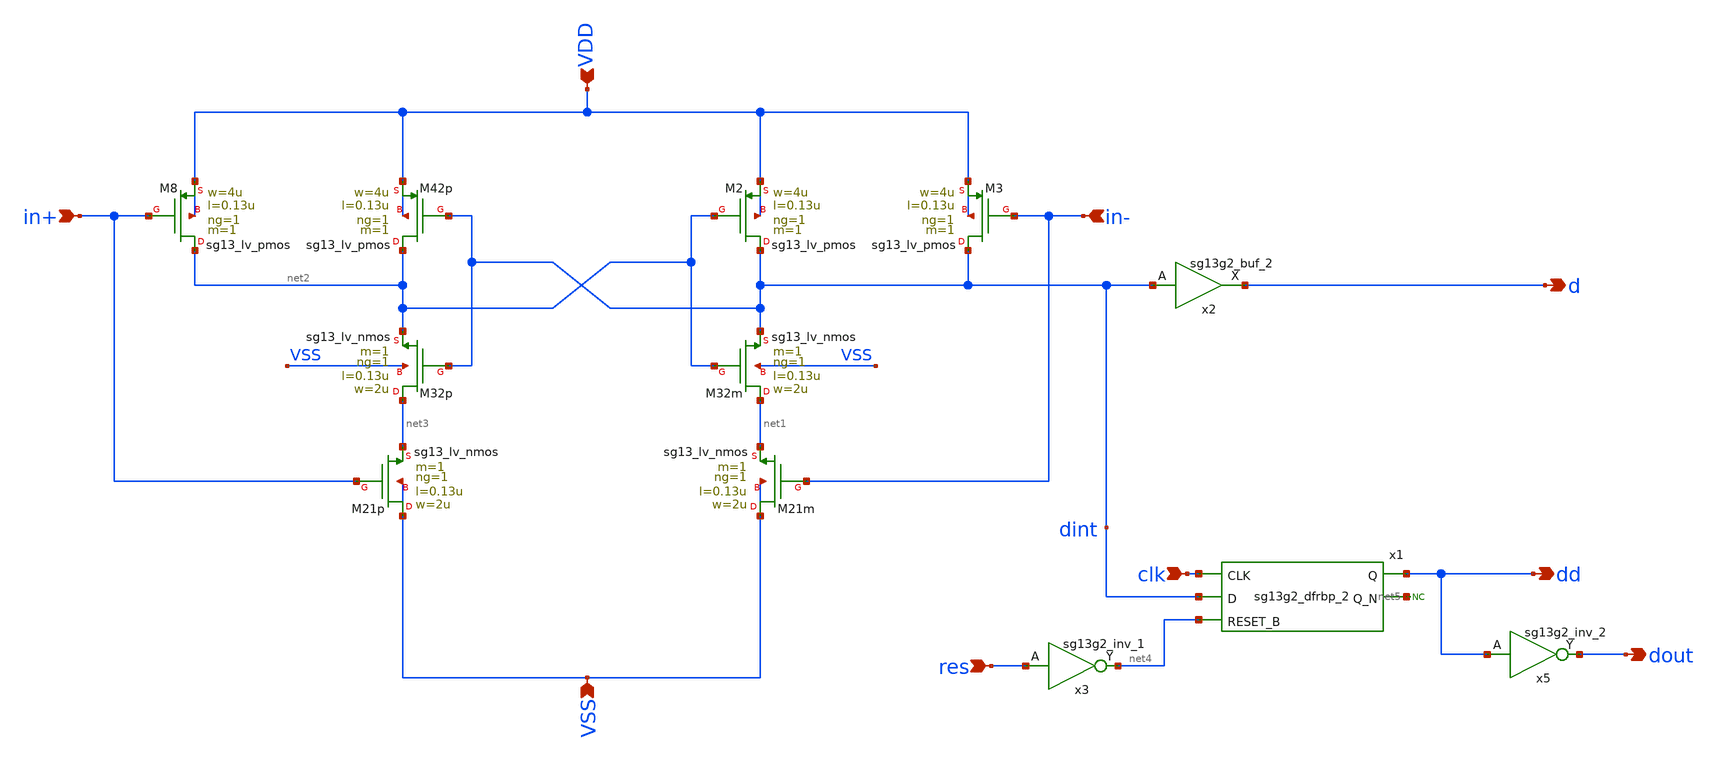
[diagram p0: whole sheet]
** sch_path: design/design_comp/latch_stage_test.sch
* IHP-GmbH/IHP-Open-PDK/ihp-sg13g2/libs.tech/xschem/sg13g2_stdcells/sg13g2_inv_2.sch:
* Copyright 2023 IHP PDK Authors
* Licensed under the Apache License, Version 2.0 (the "License");
**.subckt latch_stage_test d res dd dout in+ in- VDD VSS clk
*.opin d
*.ipin res
*.opin dd
*.opin dout
*.ipin in+
*.ipin in-
*.ipin VDD
*.ipin VSS
*.ipin clk
XM32m net1 net2 dint VSS sg13_lv_nmos w=2u l=0.13u ng=1 m=1 mm_ok=1
XM2 dint net2 VDD VDD sg13_lv_pmos w=4u l=0.13u ng=1 m=1 mm_ok=1
XM3 dint in- VDD VDD sg13_lv_pmos w=4u l=0.13u ng=1 m=1 mm_ok=1
XM21m VSS in- net1 VSS sg13_lv_nmos w=2u l=0.13u ng=1 m=1 mm_ok=1
XM32p net3 dint net2 VSS sg13_lv_nmos w=2u l=0.13u ng=1 m=1 mm_ok=1
XM42p net2 dint VDD VDD sg13_lv_pmos w=4u l=0.13u ng=1 m=1 mm_ok=1
XM8 net2 in+ VDD VDD sg13_lv_pmos w=4u l=0.13u ng=1 m=1 mm_ok=1
XM21p VSS in+ net3 VSS sg13_lv_nmos w=2u l=0.13u ng=1 m=1 mm_ok=1
x1 dd net5 clk dint net4 VDD VSS sg13g2_dfrbp_2
x2 d dint VDD VSS sg13g2_buf_2
x3 net4 res VDD VSS sg13g2_inv_1
x5 dout dd VDD VSS sg13g2_inv_2
* noconn #net5
**.ends

* expanding   symbol:  sg13g2_stdcells/sg13g2_dfrbp_2.sym # of pins=5
** sym_path: sg13g2_stdcells/sg13g2_dfrbp_2.sym
** sch_path: sg13g2_stdcells/sg13g2_dfrbp_2.sch
.subckt sg13g2_dfrbp_2 Q Q_N CLK D RESET_B VDD VSS
*.ipin D
*.ipin RESET_B
*.ipin CLK
*.opin Q
*.opin Q_N
*.iopin VDD
*.iopin VSS
XM1 Db D net12 VSS sg13_lv_nmos w=420.00n l=130.00n ng=1 m=1 mm_ok=1
XM2 net12 RESET_B VSS VSS sg13_lv_nmos w=420.00n l=130.00n ng=1 m=1 mm_ok=1
XM3 net2 clkneg net11 VSS sg13_lv_nmos w=420.00n l=130.00n ng=1 m=1 mm_ok=1
XM4 net11 net3 VSS VSS sg13_lv_nmos w=420.00n l=130.00n ng=1 m=1 mm_ok=1
XM5 net3 net2 net7 VSS sg13_lv_nmos w=420.00n l=130.00n ng=1 m=1 mm_ok=1
XM6 net7 RESET_B VSS VSS sg13_lv_nmos w=420.00n l=130.00n ng=1 m=1 mm_ok=1
XM7 Q_N net2 VSS VSS sg13_lv_nmos w=1.48u l=130.00n ng=2 m=1 mm_ok=1
XM8 net1 net2 VSS VSS sg13_lv_nmos w=640.00n l=130.00n ng=1 m=1 mm_ok=1
XM9 Q net1 VSS VSS sg13_lv_nmos w=1.48u l=130.00n ng=2 m=1 mm_ok=1
XM10 clkneg CLK VSS VSS sg13_lv_nmos w=740.00n l=130.00n ng=1 m=1 mm_ok=1
XM11 clkpos clkneg VSS VSS sg13_lv_nmos w=740.00n l=130.00n ng=1 m=1 mm_ok=1
XM12 Db clkneg net4 VSS sg13_lv_nmos w=420.00n l=130.00n ng=1 m=1 mm_ok=1
XM13 net4 clkpos net10 VSS sg13_lv_nmos w=420.00n l=130.00n ng=1 m=1 mm_ok=1
XM14 net10 net5 net6 VSS sg13_lv_nmos w=420.00n l=130.00n ng=1 m=1 mm_ok=1
XM15 net6 RESET_B VSS VSS sg13_lv_nmos w=420.00n l=130.00n ng=1 m=1 mm_ok=1
XM16 net5 net4 VSS VSS sg13_lv_nmos w=740.00n l=130.00n ng=1 m=1 mm_ok=1
XM17 net5 clkpos net2 VSS sg13_lv_nmos w=740.00n l=130.00n ng=1 m=1 mm_ok=1
XM18 Db RESET_B VDD VDD sg13_lv_pmos w=420.00n l=130.00n ng=1 m=1 mm_ok=1
XM19 Db D VDD VDD sg13_lv_pmos w=420.00n l=130.00n ng=1 m=1 mm_ok=1
XM20 net9 net3 VDD VDD sg13_lv_pmos w=420.00n l=130.00n ng=1 m=1 mm_ok=1
XM21 net2 clkpos net9 VDD sg13_lv_pmos w=420.00n l=130.00n ng=1 m=1 mm_ok=1
XM22 net3 net2 VDD VDD sg13_lv_pmos w=420.00n l=130.00n ng=1 m=1 mm_ok=1
XM23 net3 RESET_B VDD VDD sg13_lv_pmos w=420.00n l=130.00n ng=1 m=1 mm_ok=1
XM24 Q_N net2 VDD VDD sg13_lv_pmos w=2.24u l=130.00n ng=2 m=1 mm_ok=1
XM25 net1 net2 VDD VDD sg13_lv_pmos w=1.000u l=130.00n ng=1 m=1 mm_ok=1
XM26 Q net1 VDD VDD sg13_lv_pmos w=2.24u l=130.00n ng=2 m=1 mm_ok=1
XM27 clkneg CLK VDD VDD sg13_lv_pmos w=1.12u l=130.00n ng=1 m=1 mm_ok=1
XM28 clkpos clkneg VDD VDD sg13_lv_pmos w=1.12u l=130.00n ng=1 m=1 mm_ok=1
XM29 Db clkpos net4 VDD sg13_lv_pmos w=420.00n l=130.00n ng=1 m=1 mm_ok=1
XM30 net8 net5 VDD VDD sg13_lv_pmos w=420.00n l=130.00n ng=1 m=1 mm_ok=1
XM31 net4 clkneg net8 VDD sg13_lv_pmos w=420.00n l=130.00n ng=1 m=1 mm_ok=1
XM32 net4 RESET_B VDD VDD sg13_lv_pmos w=420.00n l=130.00n ng=1 m=1 mm_ok=1
XM33 net5 net4 VDD VDD sg13_lv_pmos w=1.000u l=130.00n ng=1 m=1 mm_ok=1
XM34 net5 clkneg net2 VDD sg13_lv_pmos w=1.000u l=130.00n ng=1 m=1 mm_ok=1
.ends


* expanding   symbol:  sg13g2_stdcells/sg13g2_buf_2.sym # of pins=2
** sym_path: sg13g2_stdcells/sg13g2_buf_2.sym
** sch_path: sg13g2_stdcells/sg13g2_buf_2.sch
.subckt sg13g2_buf_2 X A VDD VSS
*.ipin A
*.opin X
*.iopin VDD
*.iopin VSS
XM1 net1 A VSS VSS sg13_lv_nmos w=640.00n l=130.00n ng=1 m=1 mm_ok=1
XM2 X net1 VSS VSS sg13_lv_nmos w=1.48u l=130.00n ng=2 m=1 mm_ok=1
XM3 net1 A VDD VDD sg13_lv_pmos w=1.000u l=130.00n ng=1 m=1 mm_ok=1
XM4 X net1 VDD VDD sg13_lv_pmos w=2.24u l=130.00n ng=2 m=1 mm_ok=1
.ends


* expanding   symbol:  sg13g2_stdcells/sg13g2_inv_1.sym # of pins=2
** sym_path: sg13g2_stdcells/sg13g2_inv_1.sym
** sch_path: sg13g2_stdcells/sg13g2_inv_1.sch
.subckt sg13g2_inv_1 Y A VDD VSS
*.opin Y
*.ipin A
*.iopin VDD
*.iopin VSS
XM1 Y A VSS VSS sg13_lv_nmos w=740.00n l=130.00n ng=1 m=1 mm_ok=1
XM2 Y A VDD VDD sg13_lv_pmos w=1.12u l=130.00n ng=1 m=1 mm_ok=1
.ends


* expanding   symbol:  sg13g2_stdcells/sg13g2_inv_2.sym # of pins=2
** sym_path: sg13g2_stdcells/sg13g2_inv_2.sym
** sch_path: sg13g2_stdcells/sg13g2_inv_2.sch
.subckt sg13g2_inv_2 Y A VDD VSS
*.opin Y
*.ipin A
*.iopin VDD
*.iopin VSS
XM1 Y A VSS VSS sg13_lv_nmos w=1.48u l=130.00n ng=2 m=1 mm_ok=1
XM2 Y A VDD VDD sg13_lv_pmos w=2.24u l=130.00n ng=2 m=1 mm_ok=1
.ends

.end
